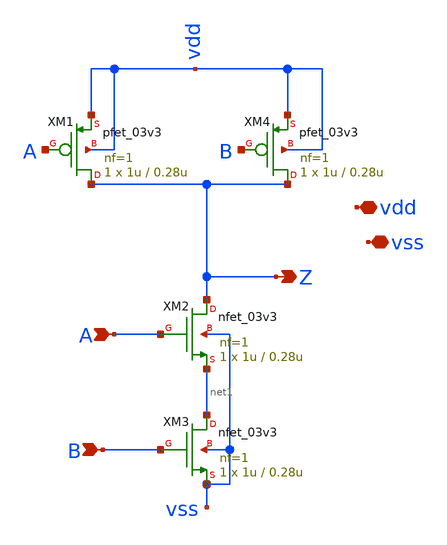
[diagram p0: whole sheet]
** sch_path: designs/libs/core_LIF_comp/core_nand/nand.sch
**.subckt nand vdd vss A Z B
*.iopin vdd
*.iopin vss
*.ipin A
*.opin Z
*.ipin B
XM1 Z A vdd vdd pfet_03v3 L=0.28u W=1u nf=1 ad='int((nf+1)/2) * W/nf * 0.18u' as='int((nf+2)/2) * W/nf * 0.18u'
+ pd='2*int((nf+1)/2) * (W/nf + 0.18u)' ps='2*int((nf+2)/2) * (W/nf + 0.18u)' nrd='0.18u / W' nrs='0.18u / W'
+ sa=0 sb=0 sd=0 m=1
XM3 net1 B vss vss nfet_03v3 L=0.28u W=1u nf=1 ad='int((nf+1)/2) * W/nf * 0.18u' as='int((nf+2)/2) * W/nf * 0.18u'
+ pd='2*int((nf+1)/2) * (W/nf + 0.18u)' ps='2*int((nf+2)/2) * (W/nf + 0.18u)' nrd='0.18u / W' nrs='0.18u / W'
+ sa=0 sb=0 sd=0 m=1
XM2 Z A net1 vss nfet_03v3 L=0.28u W=1u nf=1 ad='int((nf+1)/2) * W/nf * 0.18u' as='int((nf+2)/2) * W/nf * 0.18u'
+ pd='2*int((nf+1)/2) * (W/nf + 0.18u)' ps='2*int((nf+2)/2) * (W/nf + 0.18u)' nrd='0.18u / W' nrs='0.18u / W'
+ sa=0 sb=0 sd=0 m=1
XM4 Z B vdd vdd pfet_03v3 L=0.28u W=1u nf=1 ad='int((nf+1)/2) * W/nf * 0.18u' as='int((nf+2)/2) * W/nf * 0.18u'
+ pd='2*int((nf+1)/2) * (W/nf + 0.18u)' ps='2*int((nf+2)/2) * (W/nf + 0.18u)' nrd='0.18u / W' nrs='0.18u / W'
+ sa=0 sb=0 sd=0 m=1
**.ends
.end
